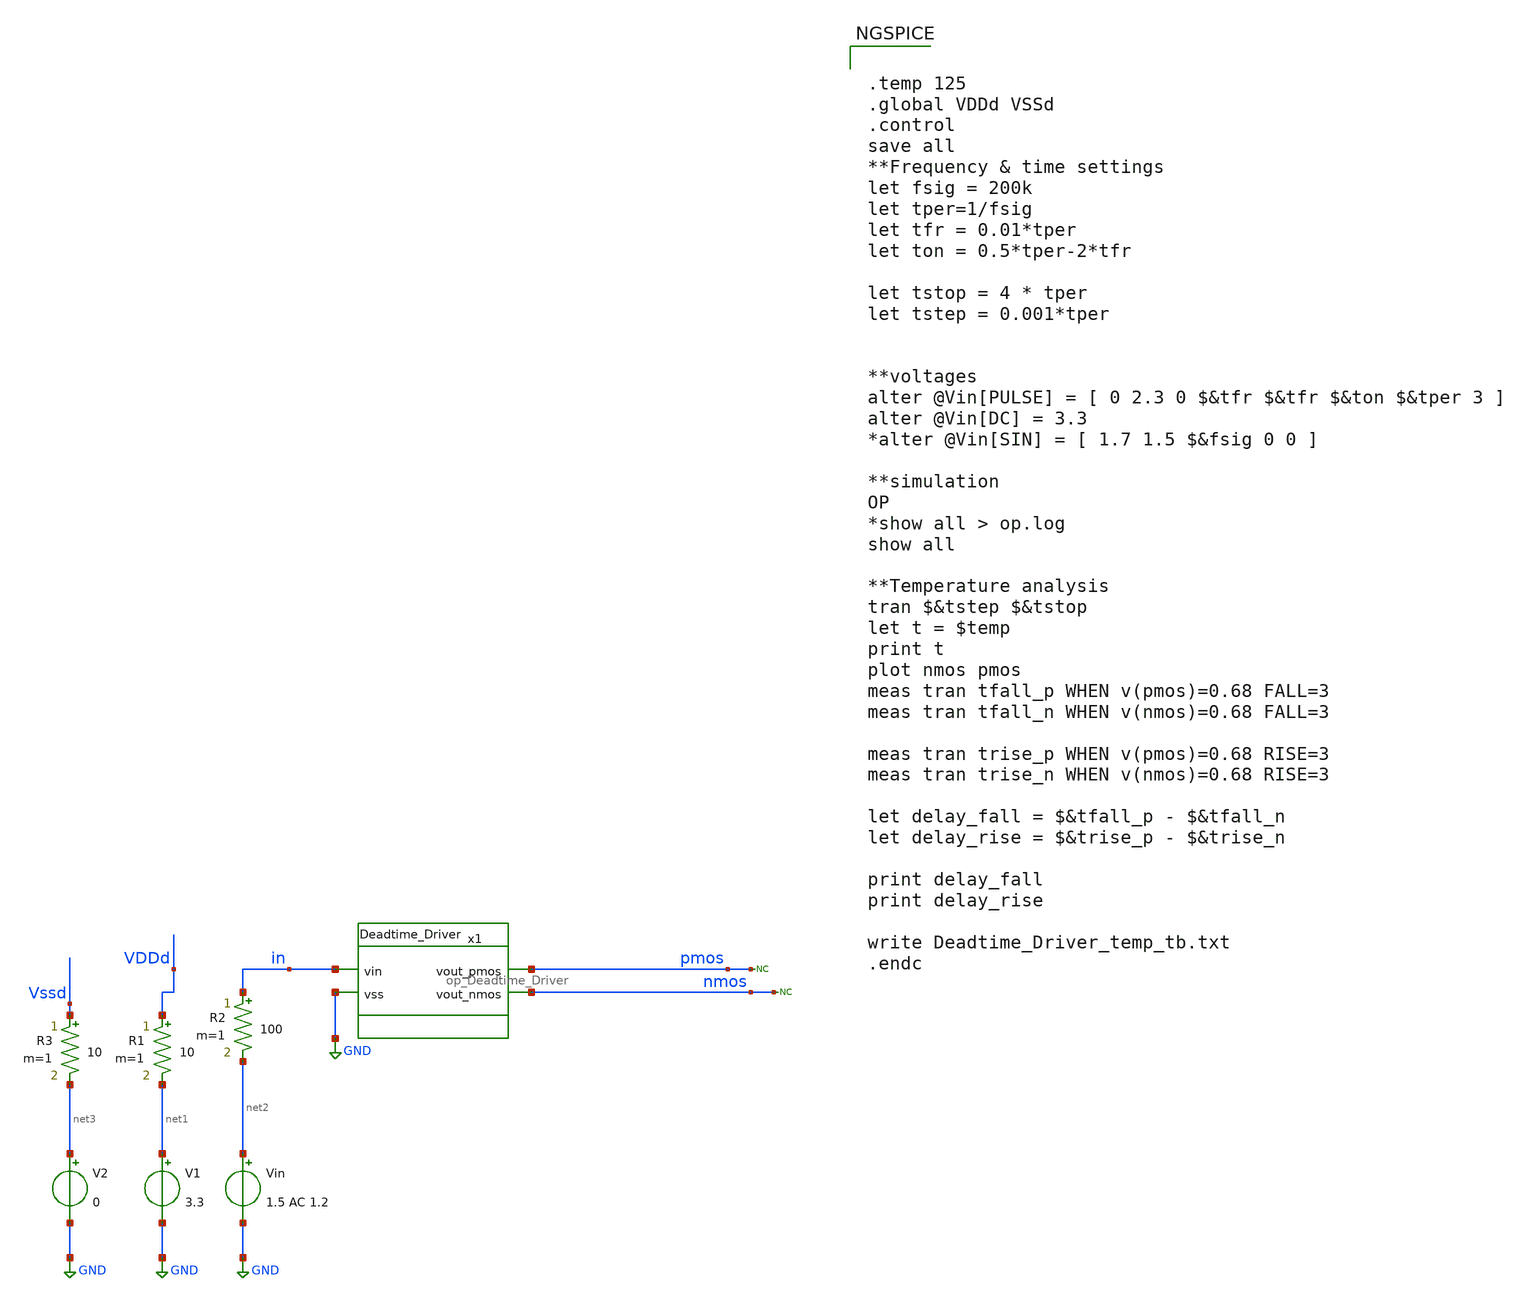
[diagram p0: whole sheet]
** sch_path: designs/libs/tb_analog/tb_op_Deadtime_Driver/tb_temp_deadtime_driver.sch
**.subckt tb_temp_deadtime_driver
V1 net1 GND 3.3
Vin net2 GND 1.5 AC 1.2
R1 VDDd net1 10 m=1
R2 in net2 100 m=1
V2 net3 GND 0
* noconn pmos
* noconn nmos
R3 Vssd net3 10 m=1
x1 pmos in nmos GND op_Deadtime_Driver
**** begin user architecture code

.include $::180MCU_MODELS/design.ngspice
.include /foss/pdks/gf180mcuD/libs.ref/gf180mcu_fd_sc_mcu9t5v0/spice/gf180mcu_fd_sc_mcu9t5v0.spice
.lib $::180MCU_MODELS/sm141064.ngspice typical
.lib $::180MCU_MODELS/sm141064.ngspice cap_mim
.lib $::180MCU_MODELS/sm141064.ngspice mimcap_typical



.temp 125
.global VDDd VSSd
.control
save all
**Frequency & time settings
let fsig = 200k
let tper=1/fsig
let tfr = 0.01*tper
let ton = 0.5*tper-2*tfr

let tstop = 4 * tper
let tstep = 0.001*tper


**voltages
alter @Vin[PULSE] = [ 0 2.3 0 $&tfr $&tfr $&ton $&tper 3 ]
alter @Vin[DC] = 3.3
*alter @Vin[SIN] = [ 1.7 1.5 $&fsig 0 0 ]

**simulation
OP
*show all > op.log
show all

**Temperature analysis
tran $&tstep $&tstop
let t = $temp
print t
plot nmos pmos
meas tran tfall_p WHEN v(pmos)=0.68 FALL=3
meas tran tfall_n WHEN v(nmos)=0.68 FALL=3

meas tran trise_p WHEN v(pmos)=0.68 RISE=3
meas tran trise_n WHEN v(nmos)=0.68 RISE=3

let delay_fall = $&tfall_p - $&tfall_n
let delay_rise = $&trise_p - $&trise_n

print delay_fall
print delay_rise

write Deadtime_Driver_temp_tb.txt
.endc


**** end user architecture code
**.ends
.GLOBAL GND
.end
